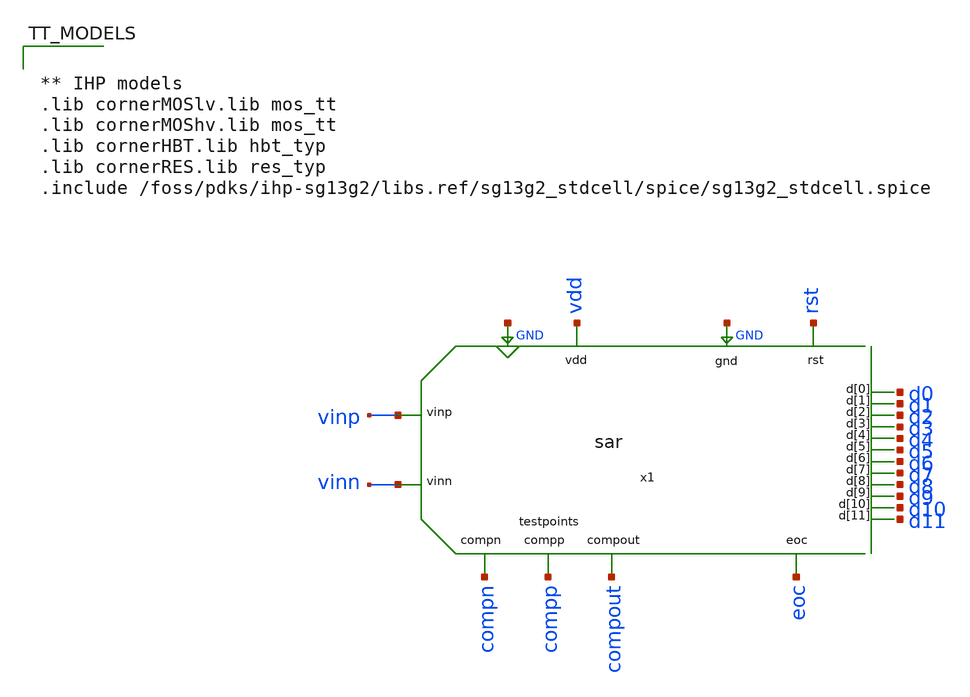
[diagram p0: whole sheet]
** sch_path: xschem/SAR_ADC/testbench/tb_sar_adc_dnl_inl.sch
**.subckt tb_sar_adc_dnl_inl
x1 vinp rst GND vinn GND vdd compn compp compout eoc d9 d7 d0 d11 d3 d4 d2 d1 d8 d6 d5 d10 sar
**** begin user architecture code

* Simulación para caracterización DNL/INL de ADC SAR 12-bit
* Barrido DC con simulación transitoria en cada punto

.param vcm=0.9
.param vdd=1.8
.param period=5n
.param conv_time=100n

* Parámetro para barrido DC
.param vdiff_sweep=0

* Fuentes de alimentación
VDD VDD 0 DC {vdd}
VSS VSS 0 DC 0

* Fuentes de entrada diferencial (mantienen Vcm constante)
Vvinp vinp 0 DC {vcm + vdiff_sweep/2}
Vvinn vinn 0 DC {vcm - vdiff_sweep/2}

* Reset: pulso inicial para iniciar conversión
Vrst rst 0 PULSE({vdd} 0 {period} 0.1n 0.1n {conv_time} {conv_time*2})

* Opciones de simulación
.options savecurrents klu method=gear reltol=1e-3 abstol=1e-12 gmin=1e-15

.control
.log logfile.txt
* Crear archivo de salida
set wr_singlescale
set wr_vecnames

* Barrido DC: 4096 puntos de -1.8V a +1.8V
let vdiff_start = -1.8
let vdiff_stop = 1.8
let n_points = 16
let vdiff_step = (vdiff_stop - vdiff_start) / (n_points - 1)

* Vectores para almacenar resultados
let vdiff_vec = unitvec(n_points)
let vinp_vec = unitvec(n_points)
let vinn_vec = unitvec(n_points)
let b0_vec = unitvec(n_points)
let b1_vec = unitvec(n_points)
let b2_vec = unitvec(n_points)
let b3_vec = unitvec(n_points)
let b4_vec = unitvec(n_points)
let b5_vec = unitvec(n_points)
let b6_vec = unitvec(n_points)
let b7_vec = unitvec(n_points)
let b8_vec = unitvec(n_points)
let b9_vec = unitvec(n_points)
let b10_vec = unitvec(n_points)
let b11_vec = unitvec(n_points)
let eoc_vec = unitvec(n_points)

* Loop del barrido
let idx = 0
let vdiff_val = vdiff_start

while idx < n_points
    * Configurar voltaje diferencial para este punto
    alter vvinp = vcm + vdiff_val/2
    alter vvinn = vcm - vdiff_val/2

    * Ejecutar simulación transitoria
    tran 0.05n 120n

    * Guardar vectores actuales antes de que se pierdan
    let time_tmp = time
    let eoc_tmp = eoc
    let vinp_tmp = vinp
    let vinn_tmp = vinn
    let b0_tmp = b0
    let b1_tmp = b1
    let b2_tmp = b2
    let b3_tmp = b3
    let b4_tmp = b4
    let b5_tmp = b5
    let b6_tmp = b6
    let b7_tmp = b7
    let b8_tmp = b8
    let b9_tmp = b9
    let b10_tmp = b10
    let b11_tmp = b11

    * Buscar el momento donde eoc está alto
    let eoc_high = eoc_tmp > 0.9
    let last_idx = length(time_tmp) - 1

    * Mientras eoc no esté alto, retroceder en el tiempo
    while eoc_high[last_idx] < 0.5
        let last_idx = last_idx - 1
        if last_idx < 1
            break
        end
    end

    * Guardar valores en este punto
    let vdiff_vec[idx] = vdiff_val
    let vinp_vec[idx] = vinp_tmp[last_idx]
    let vinn_vec[idx] = vinn_tmp[last_idx]
    let b0_vec[idx] = b0_tmp[last_idx]
    let b1_vec[idx] = b1_tmp[last_idx]
    let b2_vec[idx] = b2_tmp[last_idx]
    let b3_vec[idx] = b3_tmp[last_idx]
    let b4_vec[idx] = b4_tmp[last_idx]
    let b5_vec[idx] = b5_tmp[last_idx]
    let b6_vec[idx] = b6_tmp[last_idx]
    let b7_vec[idx] = b7_tmp[last_idx]
    let b8_vec[idx] = b8_tmp[last_idx]
    let b9_vec[idx] = b9_tmp[last_idx]
    let b10_vec[idx] = b10_tmp[last_idx]
    let b11_vec[idx] = b11_tmp[last_idx]
    let eoc_vec[idx] = eoc_tmp[last_idx]


    * Siguiente punto
    let idx = idx + 1
    let vdiff_val = vdiff_val + vdiff_step

    * Limpiar vectores temporales
    destroy time_tmp eoc_tmp vinp_tmp vinn_tmp b0_tmp b1_tmp b2_tmp b3_tmp b4_tmp b5_tmp b6_tmp
+ b7_tmp b8_tmp b9_tmp b10_tmp b11_tmp
end

* Guardar resultados
write dnl_inl_data.raw vdiff_vec vinp_vec vinn_vec b0_vec b1_vec b2_vec b3_vec b4_vec b5_vec b6_vec
+ b7_vec b8_vec b9_vec b10_vec b11_vec eoc_vec

.endc



** IHP models
.lib cornerMOSlv.lib mos_tt
.lib cornerMOShv.lib mos_tt
.lib cornerHBT.lib hbt_typ
.lib cornerRES.lib res_typ
.include /foss/pdks/ihp-sg13g2/libs.ref/sg13g2_stdcell/spice/sg13g2_stdcell.spice


**** end user architecture code
**.ends
.GLOBAL GND
.end
